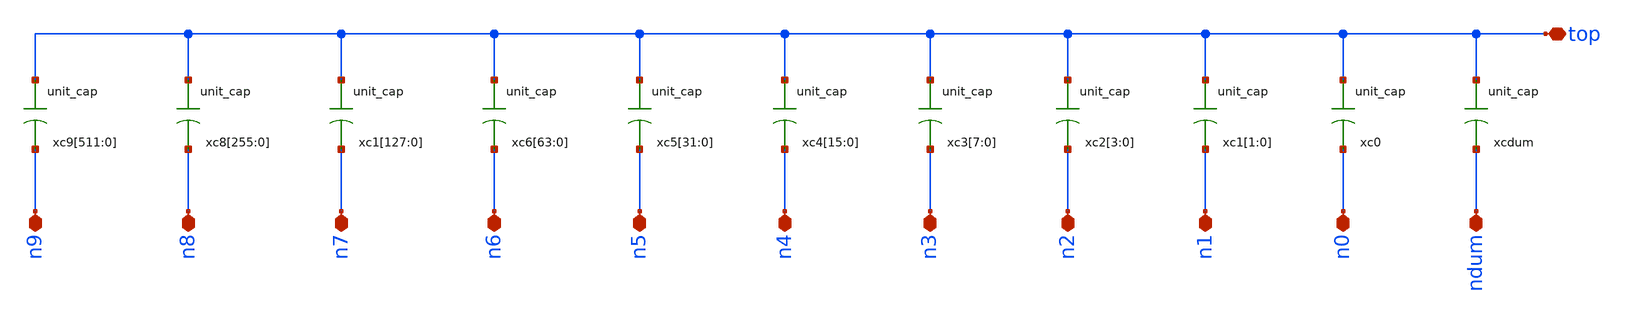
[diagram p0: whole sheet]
** sch_path: xschem/adc/carry.sch
**.subckt carry n9 n8 n7 n6 n5 n4 n3 n2 n1 n0 ndum top
*.iopin n9
*.iopin n8
*.iopin n7
*.iopin n6
*.iopin n5
*.iopin n4
*.iopin n3
*.iopin n2
*.iopin n1
*.iopin n0
*.iopin ndum
*.iopin top
xc9[511] top n9 unit_cap
xc9[510] top n9 unit_cap
xc9[509] top n9 unit_cap
xc9[508] top n9 unit_cap
xc9[507] top n9 unit_cap
xc9[506] top n9 unit_cap
xc9[505] top n9 unit_cap
xc9[504] top n9 unit_cap
xc9[503] top n9 unit_cap
xc9[502] top n9 unit_cap
xc9[501] top n9 unit_cap
xc9[500] top n9 unit_cap
xc9[499] top n9 unit_cap
xc9[498] top n9 unit_cap
xc9[497] top n9 unit_cap
xc9[496] top n9 unit_cap
xc9[495] top n9 unit_cap
xc9[494] top n9 unit_cap
xc9[493] top n9 unit_cap
xc9[492] top n9 unit_cap
xc9[491] top n9 unit_cap
xc9[490] top n9 unit_cap
xc9[489] top n9 unit_cap
xc9[488] top n9 unit_cap
xc9[487] top n9 unit_cap
xc9[486] top n9 unit_cap
xc9[485] top n9 unit_cap
xc9[484] top n9 unit_cap
xc9[483] top n9 unit_cap
xc9[482] top n9 unit_cap
xc9[481] top n9 unit_cap
xc9[480] top n9 unit_cap
xc9[479] top n9 unit_cap
xc9[478] top n9 unit_cap
xc9[477] top n9 unit_cap
xc9[476] top n9 unit_cap
xc9[475] top n9 unit_cap
xc9[474] top n9 unit_cap
xc9[473] top n9 unit_cap
xc9[472] top n9 unit_cap
xc9[471] top n9 unit_cap
xc9[470] top n9 unit_cap
xc9[469] top n9 unit_cap
xc9[468] top n9 unit_cap
xc9[467] top n9 unit_cap
xc9[466] top n9 unit_cap
xc9[465] top n9 unit_cap
xc9[464] top n9 unit_cap
xc9[463] top n9 unit_cap
xc9[462] top n9 unit_cap
xc9[461] top n9 unit_cap
xc9[460] top n9 unit_cap
xc9[459] top n9 unit_cap
xc9[458] top n9 unit_cap
xc9[457] top n9 unit_cap
xc9[456] top n9 unit_cap
xc9[455] top n9 unit_cap
xc9[454] top n9 unit_cap
xc9[453] top n9 unit_cap
xc9[452] top n9 unit_cap
xc9[451] top n9 unit_cap
xc9[450] top n9 unit_cap
xc9[449] top n9 unit_cap
xc9[448] top n9 unit_cap
xc9[447] top n9 unit_cap
xc9[446] top n9 unit_cap
xc9[445] top n9 unit_cap
xc9[444] top n9 unit_cap
xc9[443] top n9 unit_cap
xc9[442] top n9 unit_cap
xc9[441] top n9 unit_cap
xc9[440] top n9 unit_cap
xc9[439] top n9 unit_cap
xc9[438] top n9 unit_cap
xc9[437] top n9 unit_cap
xc9[436] top n9 unit_cap
xc9[435] top n9 unit_cap
xc9[434] top n9 unit_cap
xc9[433] top n9 unit_cap
xc9[432] top n9 unit_cap
xc9[431] top n9 unit_cap
xc9[430] top n9 unit_cap
xc9[429] top n9 unit_cap
xc9[428] top n9 unit_cap
xc9[427] top n9 unit_cap
xc9[426] top n9 unit_cap
xc9[425] top n9 unit_cap
xc9[424] top n9 unit_cap
xc9[423] top n9 unit_cap
xc9[422] top n9 unit_cap
xc9[421] top n9 unit_cap
xc9[420] top n9 unit_cap
xc9[419] top n9 unit_cap
xc9[418] top n9 unit_cap
xc9[417] top n9 unit_cap
xc9[416] top n9 unit_cap
xc9[415] top n9 unit_cap
xc9[414] top n9 unit_cap
xc9[413] top n9 unit_cap
xc9[412] top n9 unit_cap
xc9[411] top n9 unit_cap
xc9[410] top n9 unit_cap
xc9[409] top n9 unit_cap
xc9[408] top n9 unit_cap
xc9[407] top n9 unit_cap
xc9[406] top n9 unit_cap
xc9[405] top n9 unit_cap
xc9[404] top n9 unit_cap
xc9[403] top n9 unit_cap
xc9[402] top n9 unit_cap
xc9[401] top n9 unit_cap
xc9[400] top n9 unit_cap
xc9[399] top n9 unit_cap
xc9[398] top n9 unit_cap
xc9[397] top n9 unit_cap
xc9[396] top n9 unit_cap
xc9[395] top n9 unit_cap
xc9[394] top n9 unit_cap
xc9[393] top n9 unit_cap
xc9[392] top n9 unit_cap
xc9[391] top n9 unit_cap
xc9[390] top n9 unit_cap
xc9[389] top n9 unit_cap
xc9[388] top n9 unit_cap
xc9[387] top n9 unit_cap
xc9[386] top n9 unit_cap
xc9[385] top n9 unit_cap
xc9[384] top n9 unit_cap
xc9[383] top n9 unit_cap
xc9[382] top n9 unit_cap
xc9[381] top n9 unit_cap
xc9[380] top n9 unit_cap
xc9[379] top n9 unit_cap
xc9[378] top n9 unit_cap
xc9[377] top n9 unit_cap
xc9[376] top n9 unit_cap
xc9[375] top n9 unit_cap
xc9[374] top n9 unit_cap
xc9[373] top n9 unit_cap
xc9[372] top n9 unit_cap
xc9[371] top n9 unit_cap
xc9[370] top n9 unit_cap
xc9[369] top n9 unit_cap
xc9[368] top n9 unit_cap
xc9[367] top n9 unit_cap
xc9[366] top n9 unit_cap
xc9[365] top n9 unit_cap
xc9[364] top n9 unit_cap
xc9[363] top n9 unit_cap
xc9[362] top n9 unit_cap
xc9[361] top n9 unit_cap
xc9[360] top n9 unit_cap
xc9[359] top n9 unit_cap
xc9[358] top n9 unit_cap
xc9[357] top n9 unit_cap
xc9[356] top n9 unit_cap
xc9[355] top n9 unit_cap
xc9[354] top n9 unit_cap
xc9[353] top n9 unit_cap
xc9[352] top n9 unit_cap
xc9[351] top n9 unit_cap
xc9[350] top n9 unit_cap
xc9[349] top n9 unit_cap
xc9[348] top n9 unit_cap
xc9[347] top n9 unit_cap
xc9[346] top n9 unit_cap
xc9[345] top n9 unit_cap
xc9[344] top n9 unit_cap
xc9[343] top n9 unit_cap
xc9[342] top n9 unit_cap
xc9[341] top n9 unit_cap
xc9[340] top n9 unit_cap
xc9[339] top n9 unit_cap
xc9[338] top n9 unit_cap
xc9[337] top n9 unit_cap
xc9[336] top n9 unit_cap
xc9[335] top n9 unit_cap
xc9[334] top n9 unit_cap
xc9[333] top n9 unit_cap
xc9[332] top n9 unit_cap
xc9[331] top n9 unit_cap
xc9[330] top n9 unit_cap
xc9[329] top n9 unit_cap
xc9[328] top n9 unit_cap
xc9[327] top n9 unit_cap
xc9[326] top n9 unit_cap
xc9[325] top n9 unit_cap
xc9[324] top n9 unit_cap
xc9[323] top n9 unit_cap
xc9[322] top n9 unit_cap
xc9[321] top n9 unit_cap
xc9[320] top n9 unit_cap
xc9[319] top n9 unit_cap
xc9[318] top n9 unit_cap
xc9[317] top n9 unit_cap
xc9[316] top n9 unit_cap
xc9[315] top n9 unit_cap
xc9[314] top n9 unit_cap
xc9[313] top n9 unit_cap
xc9[312] top n9 unit_cap
xc9[311] top n9 unit_cap
xc9[310] top n9 unit_cap
xc9[309] top n9 unit_cap
xc9[308] top n9 unit_cap
xc9[307] top n9 unit_cap
xc9[306] top n9 unit_cap
xc9[305] top n9 unit_cap
xc9[304] top n9 unit_cap
xc9[303] top n9 unit_cap
xc9[302] top n9 unit_cap
xc9[301] top n9 unit_cap
xc9[300] top n9 unit_cap
xc9[299] top n9 unit_cap
xc9[298] top n9 unit_cap
xc9[297] top n9 unit_cap
xc9[296] top n9 unit_cap
xc9[295] top n9 unit_cap
xc9[294] top n9 unit_cap
xc9[293] top n9 unit_cap
xc9[292] top n9 unit_cap
xc9[291] top n9 unit_cap
xc9[290] top n9 unit_cap
xc9[289] top n9 unit_cap
xc9[288] top n9 unit_cap
xc9[287] top n9 unit_cap
xc9[286] top n9 unit_cap
xc9[285] top n9 unit_cap
xc9[284] top n9 unit_cap
xc9[283] top n9 unit_cap
xc9[282] top n9 unit_cap
xc9[281] top n9 unit_cap
xc9[280] top n9 unit_cap
xc9[279] top n9 unit_cap
xc9[278] top n9 unit_cap
xc9[277] top n9 unit_cap
xc9[276] top n9 unit_cap
xc9[275] top n9 unit_cap
xc9[274] top n9 unit_cap
xc9[273] top n9 unit_cap
xc9[272] top n9 unit_cap
xc9[271] top n9 unit_cap
xc9[270] top n9 unit_cap
xc9[269] top n9 unit_cap
xc9[268] top n9 unit_cap
xc9[267] top n9 unit_cap
xc9[266] top n9 unit_cap
xc9[265] top n9 unit_cap
xc9[264] top n9 unit_cap
xc9[263] top n9 unit_cap
xc9[262] top n9 unit_cap
xc9[261] top n9 unit_cap
xc9[260] top n9 unit_cap
xc9[259] top n9 unit_cap
xc9[258] top n9 unit_cap
xc9[257] top n9 unit_cap
xc9[256] top n9 unit_cap
xc9[255] top n9 unit_cap
xc9[254] top n9 unit_cap
xc9[253] top n9 unit_cap
xc9[252] top n9 unit_cap
xc9[251] top n9 unit_cap
xc9[250] top n9 unit_cap
xc9[249] top n9 unit_cap
xc9[248] top n9 unit_cap
xc9[247] top n9 unit_cap
xc9[246] top n9 unit_cap
xc9[245] top n9 unit_cap
xc9[244] top n9 unit_cap
xc9[243] top n9 unit_cap
xc9[242] top n9 unit_cap
xc9[241] top n9 unit_cap
xc9[240] top n9 unit_cap
xc9[239] top n9 unit_cap
xc9[238] top n9 unit_cap
xc9[237] top n9 unit_cap
xc9[236] top n9 unit_cap
xc9[235] top n9 unit_cap
xc9[234] top n9 unit_cap
xc9[233] top n9 unit_cap
xc9[232] top n9 unit_cap
xc9[231] top n9 unit_cap
xc9[230] top n9 unit_cap
xc9[229] top n9 unit_cap
xc9[228] top n9 unit_cap
xc9[227] top n9 unit_cap
xc9[226] top n9 unit_cap
xc9[225] top n9 unit_cap
xc9[224] top n9 unit_cap
xc9[223] top n9 unit_cap
xc9[222] top n9 unit_cap
xc9[221] top n9 unit_cap
xc9[220] top n9 unit_cap
xc9[219] top n9 unit_cap
xc9[218] top n9 unit_cap
xc9[217] top n9 unit_cap
xc9[216] top n9 unit_cap
xc9[215] top n9 unit_cap
xc9[214] top n9 unit_cap
xc9[213] top n9 unit_cap
xc9[212] top n9 unit_cap
xc9[211] top n9 unit_cap
xc9[210] top n9 unit_cap
xc9[209] top n9 unit_cap
xc9[208] top n9 unit_cap
xc9[207] top n9 unit_cap
xc9[206] top n9 unit_cap
xc9[205] top n9 unit_cap
xc9[204] top n9 unit_cap
xc9[203] top n9 unit_cap
xc9[202] top n9 unit_cap
xc9[201] top n9 unit_cap
xc9[200] top n9 unit_cap
xc9[199] top n9 unit_cap
xc9[198] top n9 unit_cap
xc9[197] top n9 unit_cap
xc9[196] top n9 unit_cap
xc9[195] top n9 unit_cap
xc9[194] top n9 unit_cap
xc9[193] top n9 unit_cap
xc9[192] top n9 unit_cap
xc9[191] top n9 unit_cap
xc9[190] top n9 unit_cap
xc9[189] top n9 unit_cap
xc9[188] top n9 unit_cap
xc9[187] top n9 unit_cap
xc9[186] top n9 unit_cap
xc9[185] top n9 unit_cap
xc9[184] top n9 unit_cap
xc9[183] top n9 unit_cap
xc9[182] top n9 unit_cap
xc9[181] top n9 unit_cap
xc9[180] top n9 unit_cap
xc9[179] top n9 unit_cap
xc9[178] top n9 unit_cap
xc9[177] top n9 unit_cap
xc9[176] top n9 unit_cap
xc9[175] top n9 unit_cap
xc9[174] top n9 unit_cap
xc9[173] top n9 unit_cap
xc9[172] top n9 unit_cap
xc9[171] top n9 unit_cap
xc9[170] top n9 unit_cap
xc9[169] top n9 unit_cap
xc9[168] top n9 unit_cap
xc9[167] top n9 unit_cap
xc9[166] top n9 unit_cap
xc9[165] top n9 unit_cap
xc9[164] top n9 unit_cap
xc9[163] top n9 unit_cap
xc9[162] top n9 unit_cap
xc9[161] top n9 unit_cap
xc9[160] top n9 unit_cap
xc9[159] top n9 unit_cap
xc9[158] top n9 unit_cap
xc9[157] top n9 unit_cap
xc9[156] top n9 unit_cap
xc9[155] top n9 unit_cap
xc9[154] top n9 unit_cap
xc9[153] top n9 unit_cap
xc9[152] top n9 unit_cap
xc9[151] top n9 unit_cap
xc9[150] top n9 unit_cap
xc9[149] top n9 unit_cap
xc9[148] top n9 unit_cap
xc9[147] top n9 unit_cap
xc9[146] top n9 unit_cap
xc9[145] top n9 unit_cap
xc9[144] top n9 unit_cap
xc9[143] top n9 unit_cap
xc9[142] top n9 unit_cap
xc9[141] top n9 unit_cap
xc9[140] top n9 unit_cap
xc9[139] top n9 unit_cap
xc9[138] top n9 unit_cap
xc9[137] top n9 unit_cap
xc9[136] top n9 unit_cap
xc9[135] top n9 unit_cap
xc9[134] top n9 unit_cap
xc9[133] top n9 unit_cap
xc9[132] top n9 unit_cap
xc9[131] top n9 unit_cap
xc9[130] top n9 unit_cap
xc9[129] top n9 unit_cap
xc9[128] top n9 unit_cap
xc9[127] top n9 unit_cap
xc9[126] top n9 unit_cap
xc9[125] top n9 unit_cap
xc9[124] top n9 unit_cap
xc9[123] top n9 unit_cap
xc9[122] top n9 unit_cap
xc9[121] top n9 unit_cap
xc9[120] top n9 unit_cap
xc9[119] top n9 unit_cap
xc9[118] top n9 unit_cap
xc9[117] top n9 unit_cap
xc9[116] top n9 unit_cap
xc9[115] top n9 unit_cap
xc9[114] top n9 unit_cap
xc9[113] top n9 unit_cap
xc9[112] top n9 unit_cap
xc9[111] top n9 unit_cap
xc9[110] top n9 unit_cap
xc9[109] top n9 unit_cap
xc9[108] top n9 unit_cap
xc9[107] top n9 unit_cap
xc9[106] top n9 unit_cap
xc9[105] top n9 unit_cap
xc9[104] top n9 unit_cap
xc9[103] top n9 unit_cap
xc9[102] top n9 unit_cap
xc9[101] top n9 unit_cap
xc9[100] top n9 unit_cap
xc9[99] top n9 unit_cap
xc9[98] top n9 unit_cap
xc9[97] top n9 unit_cap
xc9[96] top n9 unit_cap
xc9[95] top n9 unit_cap
xc9[94] top n9 unit_cap
xc9[93] top n9 unit_cap
xc9[92] top n9 unit_cap
xc9[91] top n9 unit_cap
xc9[90] top n9 unit_cap
xc9[89] top n9 unit_cap
xc9[88] top n9 unit_cap
xc9[87] top n9 unit_cap
xc9[86] top n9 unit_cap
xc9[85] top n9 unit_cap
xc9[84] top n9 unit_cap
xc9[83] top n9 unit_cap
xc9[82] top n9 unit_cap
xc9[81] top n9 unit_cap
xc9[80] top n9 unit_cap
xc9[79] top n9 unit_cap
xc9[78] top n9 unit_cap
xc9[77] top n9 unit_cap
xc9[76] top n9 unit_cap
xc9[75] top n9 unit_cap
xc9[74] top n9 unit_cap
xc9[73] top n9 unit_cap
xc9[72] top n9 unit_cap
xc9[71] top n9 unit_cap
xc9[70] top n9 unit_cap
xc9[69] top n9 unit_cap
xc9[68] top n9 unit_cap
xc9[67] top n9 unit_cap
xc9[66] top n9 unit_cap
xc9[65] top n9 unit_cap
xc9[64] top n9 unit_cap
xc9[63] top n9 unit_cap
xc9[62] top n9 unit_cap
xc9[61] top n9 unit_cap
xc9[60] top n9 unit_cap
xc9[59] top n9 unit_cap
xc9[58] top n9 unit_cap
xc9[57] top n9 unit_cap
xc9[56] top n9 unit_cap
xc9[55] top n9 unit_cap
xc9[54] top n9 unit_cap
xc9[53] top n9 unit_cap
xc9[52] top n9 unit_cap
xc9[51] top n9 unit_cap
xc9[50] top n9 unit_cap
xc9[49] top n9 unit_cap
xc9[48] top n9 unit_cap
xc9[47] top n9 unit_cap
xc9[46] top n9 unit_cap
xc9[45] top n9 unit_cap
xc9[44] top n9 unit_cap
xc9[43] top n9 unit_cap
xc9[42] top n9 unit_cap
xc9[41] top n9 unit_cap
xc9[40] top n9 unit_cap
xc9[39] top n9 unit_cap
xc9[38] top n9 unit_cap
xc9[37] top n9 unit_cap
xc9[36] top n9 unit_cap
xc9[35] top n9 unit_cap
xc9[34] top n9 unit_cap
xc9[33] top n9 unit_cap
xc9[32] top n9 unit_cap
xc9[31] top n9 unit_cap
xc9[30] top n9 unit_cap
xc9[29] top n9 unit_cap
xc9[28] top n9 unit_cap
xc9[27] top n9 unit_cap
xc9[26] top n9 unit_cap
xc9[25] top n9 unit_cap
xc9[24] top n9 unit_cap
xc9[23] top n9 unit_cap
xc9[22] top n9 unit_cap
xc9[21] top n9 unit_cap
xc9[20] top n9 unit_cap
xc9[19] top n9 unit_cap
xc9[18] top n9 unit_cap
xc9[17] top n9 unit_cap
xc9[16] top n9 unit_cap
xc9[15] top n9 unit_cap
xc9[14] top n9 unit_cap
xc9[13] top n9 unit_cap
xc9[12] top n9 unit_cap
xc9[11] top n9 unit_cap
xc9[10] top n9 unit_cap
xc9[9] top n9 unit_cap
xc9[8] top n9 unit_cap
xc9[7] top n9 unit_cap
xc9[6] top n9 unit_cap
xc9[5] top n9 unit_cap
xc9[4] top n9 unit_cap
xc9[3] top n9 unit_cap
xc9[2] top n9 unit_cap
xc9[1] top n9 unit_cap
xc9[0] top n9 unit_cap
xc8[255] top n8 unit_cap
xc8[254] top n8 unit_cap
xc8[253] top n8 unit_cap
xc8[252] top n8 unit_cap
xc8[251] top n8 unit_cap
xc8[250] top n8 unit_cap
xc8[249] top n8 unit_cap
xc8[248] top n8 unit_cap
xc8[247] top n8 unit_cap
xc8[246] top n8 unit_cap
xc8[245] top n8 unit_cap
xc8[244] top n8 unit_cap
xc8[243] top n8 unit_cap
xc8[242] top n8 unit_cap
xc8[241] top n8 unit_cap
xc8[240] top n8 unit_cap
xc8[239] top n8 unit_cap
xc8[238] top n8 unit_cap
xc8[237] top n8 unit_cap
xc8[236] top n8 unit_cap
xc8[235] top n8 unit_cap
xc8[234] top n8 unit_cap
xc8[233] top n8 unit_cap
xc8[232] top n8 unit_cap
xc8[231] top n8 unit_cap
xc8[230] top n8 unit_cap
xc8[229] top n8 unit_cap
xc8[228] top n8 unit_cap
xc8[227] top n8 unit_cap
xc8[226] top n8 unit_cap
xc8[225] top n8 unit_cap
xc8[224] top n8 unit_cap
xc8[223] top n8 unit_cap
xc8[222] top n8 unit_cap
xc8[221] top n8 unit_cap
xc8[220] top n8 unit_cap
xc8[219] top n8 unit_cap
xc8[218] top n8 unit_cap
xc8[217] top n8 unit_cap
xc8[216] top n8 unit_cap
xc8[215] top n8 unit_cap
xc8[214] top n8 unit_cap
xc8[213] top n8 unit_cap
xc8[212] top n8 unit_cap
xc8[211] top n8 unit_cap
xc8[210] top n8 unit_cap
xc8[209] top n8 unit_cap
xc8[208] top n8 unit_cap
xc8[207] top n8 unit_cap
xc8[206] top n8 unit_cap
xc8[205] top n8 unit_cap
xc8[204] top n8 unit_cap
xc8[203] top n8 unit_cap
xc8[202] top n8 unit_cap
xc8[201] top n8 unit_cap
xc8[200] top n8 unit_cap
xc8[199] top n8 unit_cap
xc8[198] top n8 unit_cap
xc8[197] top n8 unit_cap
xc8[196] top n8 unit_cap
xc8[195] top n8 unit_cap
xc8[194] top n8 unit_cap
xc8[193] top n8 unit_cap
xc8[192] top n8 unit_cap
xc8[191] top n8 unit_cap
xc8[190] top n8 unit_cap
xc8[189] top n8 unit_cap
xc8[188] top n8 unit_cap
xc8[187] top n8 unit_cap
xc8[186] top n8 unit_cap
xc8[185] top n8 unit_cap
xc8[184] top n8 unit_cap
xc8[183] top n8 unit_cap
xc8[182] top n8 unit_cap
xc8[181] top n8 unit_cap
xc8[180] top n8 unit_cap
xc8[179] top n8 unit_cap
xc8[178] top n8 unit_cap
xc8[177] top n8 unit_cap
xc8[176] top n8 unit_cap
xc8[175] top n8 unit_cap
xc8[174] top n8 unit_cap
xc8[173] top n8 unit_cap
xc8[172] top n8 unit_cap
xc8[171] top n8 unit_cap
xc8[170] top n8 unit_cap
xc8[169] top n8 unit_cap
xc8[168] top n8 unit_cap
xc8[167] top n8 unit_cap
xc8[166] top n8 unit_cap
xc8[165] top n8 unit_cap
xc8[164] top n8 unit_cap
xc8[163] top n8 unit_cap
xc8[162] top n8 unit_cap
xc8[161] top n8 unit_cap
xc8[160] top n8 unit_cap
xc8[159] top n8 unit_cap
xc8[158] top n8 unit_cap
xc8[157] top n8 unit_cap
xc8[156] top n8 unit_cap
xc8[155] top n8 unit_cap
xc8[154] top n8 unit_cap
xc8[153] top n8 unit_cap
xc8[152] top n8 unit_cap
xc8[151] top n8 unit_cap
xc8[150] top n8 unit_cap
xc8[149] top n8 unit_cap
xc8[148] top n8 unit_cap
xc8[147] top n8 unit_cap
xc8[146] top n8 unit_cap
xc8[145] top n8 unit_cap
xc8[144] top n8 unit_cap
xc8[143] top n8 unit_cap
xc8[142] top n8 unit_cap
xc8[141] top n8 unit_cap
xc8[140] top n8 unit_cap
xc8[139] top n8 unit_cap
xc8[138] top n8 unit_cap
xc8[137] top n8 unit_cap
xc8[136] top n8 unit_cap
xc8[135] top n8 unit_cap
xc8[134] top n8 unit_cap
xc8[133] top n8 unit_cap
xc8[132] top n8 unit_cap
xc8[131] top n8 unit_cap
xc8[130] top n8 unit_cap
xc8[129] top n8 unit_cap
xc8[128] top n8 unit_cap
xc8[127] top n8 unit_cap
xc8[126] top n8 unit_cap
xc8[125] top n8 unit_cap
xc8[124] top n8 unit_cap
xc8[123] top n8 unit_cap
xc8[122] top n8 unit_cap
xc8[121] top n8 unit_cap
xc8[120] top n8 unit_cap
xc8[119] top n8 unit_cap
xc8[118] top n8 unit_cap
xc8[117] top n8 unit_cap
xc8[116] top n8 unit_cap
xc8[115] top n8 unit_cap
xc8[114] top n8 unit_cap
xc8[113] top n8 unit_cap
xc8[112] top n8 unit_cap
xc8[111] top n8 unit_cap
xc8[110] top n8 unit_cap
xc8[109] top n8 unit_cap
xc8[108] top n8 unit_cap
xc8[107] top n8 unit_cap
xc8[106] top n8 unit_cap
xc8[105] top n8 unit_cap
xc8[104] top n8 unit_cap
xc8[103] top n8 unit_cap
xc8[102] top n8 unit_cap
xc8[101] top n8 unit_cap
xc8[100] top n8 unit_cap
xc8[99] top n8 unit_cap
xc8[98] top n8 unit_cap
xc8[97] top n8 unit_cap
xc8[96] top n8 unit_cap
xc8[95] top n8 unit_cap
xc8[94] top n8 unit_cap
xc8[93] top n8 unit_cap
xc8[92] top n8 unit_cap
xc8[91] top n8 unit_cap
xc8[90] top n8 unit_cap
xc8[89] top n8 unit_cap
xc8[88] top n8 unit_cap
xc8[87] top n8 unit_cap
xc8[86] top n8 unit_cap
xc8[85] top n8 unit_cap
xc8[84] top n8 unit_cap
xc8[83] top n8 unit_cap
xc8[82] top n8 unit_cap
xc8[81] top n8 unit_cap
xc8[80] top n8 unit_cap
xc8[79] top n8 unit_cap
xc8[78] top n8 unit_cap
xc8[77] top n8 unit_cap
xc8[76] top n8 unit_cap
xc8[75] top n8 unit_cap
xc8[74] top n8 unit_cap
xc8[73] top n8 unit_cap
xc8[72] top n8 unit_cap
xc8[71] top n8 unit_cap
xc8[70] top n8 unit_cap
xc8[69] top n8 unit_cap
xc8[68] top n8 unit_cap
xc8[67] top n8 unit_cap
xc8[66] top n8 unit_cap
xc8[65] top n8 unit_cap
xc8[64] top n8 unit_cap
xc8[63] top n8 unit_cap
xc8[62] top n8 unit_cap
xc8[61] top n8 unit_cap
xc8[60] top n8 unit_cap
xc8[59] top n8 unit_cap
xc8[58] top n8 unit_cap
xc8[57] top n8 unit_cap
xc8[56] top n8 unit_cap
xc8[55] top n8 unit_cap
xc8[54] top n8 unit_cap
xc8[53] top n8 unit_cap
xc8[52] top n8 unit_cap
xc8[51] top n8 unit_cap
xc8[50] top n8 unit_cap
xc8[49] top n8 unit_cap
xc8[48] top n8 unit_cap
xc8[47] top n8 unit_cap
xc8[46] top n8 unit_cap
xc8[45] top n8 unit_cap
xc8[44] top n8 unit_cap
xc8[43] top n8 unit_cap
xc8[42] top n8 unit_cap
xc8[41] top n8 unit_cap
xc8[40] top n8 unit_cap
xc8[39] top n8 unit_cap
xc8[38] top n8 unit_cap
xc8[37] top n8 unit_cap
xc8[36] top n8 unit_cap
xc8[35] top n8 unit_cap
xc8[34] top n8 unit_cap
xc8[33] top n8 unit_cap
xc8[32] top n8 unit_cap
xc8[31] top n8 unit_cap
xc8[30] top n8 unit_cap
xc8[29] top n8 unit_cap
xc8[28] top n8 unit_cap
xc8[27] top n8 unit_cap
xc8[26] top n8 unit_cap
xc8[25] top n8 unit_cap
xc8[24] top n8 unit_cap
xc8[23] top n8 unit_cap
xc8[22] top n8 unit_cap
xc8[21] top n8 unit_cap
xc8[20] top n8 unit_cap
xc8[19] top n8 unit_cap
xc8[18] top n8 unit_cap
xc8[17] top n8 unit_cap
xc8[16] top n8 unit_cap
xc8[15] top n8 unit_cap
xc8[14] top n8 unit_cap
xc8[13] top n8 unit_cap
xc8[12] top n8 unit_cap
xc8[11] top n8 unit_cap
xc8[10] top n8 unit_cap
xc8[9] top n8 unit_cap
xc8[8] top n8 unit_cap
xc8[7] top n8 unit_cap
xc8[6] top n8 unit_cap
xc8[5] top n8 unit_cap
xc8[4] top n8 unit_cap
xc8[3] top n8 unit_cap
xc8[2] top n8 unit_cap
xc8[1] top n8 unit_cap
xc8[0] top n8 unit_cap
xc0 top n0 unit_cap
xcdum top ndum unit_cap
xc1[1] top n1 unit_cap
xc1[0] top n1 unit_cap
xc2[3] top n2 unit_cap
xc2[2] top n2 unit_cap
xc2[1] top n2 unit_cap
xc2[0] top n2 unit_cap
xc3[7] top n3 unit_cap
xc3[6] top n3 unit_cap
xc3[5] top n3 unit_cap
xc3[4] top n3 unit_cap
xc3[3] top n3 unit_cap
xc3[2] top n3 unit_cap
xc3[1] top n3 unit_cap
xc3[0] top n3 unit_cap
xc4[15] top n4 unit_cap
xc4[14] top n4 unit_cap
xc4[13] top n4 unit_cap
xc4[12] top n4 unit_cap
xc4[11] top n4 unit_cap
xc4[10] top n4 unit_cap
xc4[9] top n4 unit_cap
xc4[8] top n4 unit_cap
xc4[7] top n4 unit_cap
xc4[6] top n4 unit_cap
xc4[5] top n4 unit_cap
xc4[4] top n4 unit_cap
xc4[3] top n4 unit_cap
xc4[2] top n4 unit_cap
xc4[1] top n4 unit_cap
xc4[0] top n4 unit_cap
xc5[31] top n5 unit_cap
xc5[30] top n5 unit_cap
xc5[29] top n5 unit_cap
xc5[28] top n5 unit_cap
xc5[27] top n5 unit_cap
xc5[26] top n5 unit_cap
xc5[25] top n5 unit_cap
xc5[24] top n5 unit_cap
xc5[23] top n5 unit_cap
xc5[22] top n5 unit_cap
xc5[21] top n5 unit_cap
xc5[20] top n5 unit_cap
xc5[19] top n5 unit_cap
xc5[18] top n5 unit_cap
xc5[17] top n5 unit_cap
xc5[16] top n5 unit_cap
xc5[15] top n5 unit_cap
xc5[14] top n5 unit_cap
xc5[13] top n5 unit_cap
xc5[12] top n5 unit_cap
xc5[11] top n5 unit_cap
xc5[10] top n5 unit_cap
xc5[9] top n5 unit_cap
xc5[8] top n5 unit_cap
xc5[7] top n5 unit_cap
xc5[6] top n5 unit_cap
xc5[5] top n5 unit_cap
xc5[4] top n5 unit_cap
xc5[3] top n5 unit_cap
xc5[2] top n5 unit_cap
xc5[1] top n5 unit_cap
xc5[0] top n5 unit_cap
xc6[63] top n6 unit_cap
xc6[62] top n6 unit_cap
xc6[61] top n6 unit_cap
xc6[60] top n6 unit_cap
xc6[59] top n6 unit_cap
xc6[58] top n6 unit_cap
xc6[57] top n6 unit_cap
xc6[56] top n6 unit_cap
xc6[55] top n6 unit_cap
xc6[54] top n6 unit_cap
xc6[53] top n6 unit_cap
xc6[52] top n6 unit_cap
xc6[51] top n6 unit_cap
xc6[50] top n6 unit_cap
xc6[49] top n6 unit_cap
xc6[48] top n6 unit_cap
xc6[47] top n6 unit_cap
xc6[46] top n6 unit_cap
xc6[45] top n6 unit_cap
xc6[44] top n6 unit_cap
xc6[43] top n6 unit_cap
xc6[42] top n6 unit_cap
xc6[41] top n6 unit_cap
xc6[40] top n6 unit_cap
xc6[39] top n6 unit_cap
xc6[38] top n6 unit_cap
xc6[37] top n6 unit_cap
xc6[36] top n6 unit_cap
xc6[35] top n6 unit_cap
xc6[34] top n6 unit_cap
xc6[33] top n6 unit_cap
xc6[32] top n6 unit_cap
xc6[31] top n6 unit_cap
xc6[30] top n6 unit_cap
xc6[29] top n6 unit_cap
xc6[28] top n6 unit_cap
xc6[27] top n6 unit_cap
xc6[26] top n6 unit_cap
xc6[25] top n6 unit_cap
xc6[24] top n6 unit_cap
xc6[23] top n6 unit_cap
xc6[22] top n6 unit_cap
xc6[21] top n6 unit_cap
xc6[20] top n6 unit_cap
xc6[19] top n6 unit_cap
xc6[18] top n6 unit_cap
xc6[17] top n6 unit_cap
xc6[16] top n6 unit_cap
xc6[15] top n6 unit_cap
xc6[14] top n6 unit_cap
xc6[13] top n6 unit_cap
xc6[12] top n6 unit_cap
xc6[11] top n6 unit_cap
xc6[10] top n6 unit_cap
xc6[9] top n6 unit_cap
xc6[8] top n6 unit_cap
xc6[7] top n6 unit_cap
xc6[6] top n6 unit_cap
xc6[5] top n6 unit_cap
xc6[4] top n6 unit_cap
xc6[3] top n6 unit_cap
xc6[2] top n6 unit_cap
xc6[1] top n6 unit_cap
xc6[0] top n6 unit_cap
xc1[127] top n7 unit_cap
xc1[126] top n7 unit_cap
xc1[125] top n7 unit_cap
xc1[124] top n7 unit_cap
xc1[123] top n7 unit_cap
xc1[122] top n7 unit_cap
xc1[121] top n7 unit_cap
xc1[120] top n7 unit_cap
xc1[119] top n7 unit_cap
xc1[118] top n7 unit_cap
xc1[117] top n7 unit_cap
xc1[116] top n7 unit_cap
xc1[115] top n7 unit_cap
xc1[114] top n7 unit_cap
xc1[113] top n7 unit_cap
xc1[112] top n7 unit_cap
xc1[111] top n7 unit_cap
xc1[110] top n7 unit_cap
xc1[109] top n7 unit_cap
xc1[108] top n7 unit_cap
xc1[107] top n7 unit_cap
xc1[106] top n7 unit_cap
xc1[105] top n7 unit_cap
xc1[104] top n7 unit_cap
xc1[103] top n7 unit_cap
xc1[102] top n7 unit_cap
xc1[101] top n7 unit_cap
xc1[100] top n7 unit_cap
xc1[99] top n7 unit_cap
xc1[98] top n7 unit_cap
xc1[97] top n7 unit_cap
xc1[96] top n7 unit_cap
xc1[95] top n7 unit_cap
xc1[94] top n7 unit_cap
xc1[93] top n7 unit_cap
xc1[92] top n7 unit_cap
xc1[91] top n7 unit_cap
xc1[90] top n7 unit_cap
xc1[89] top n7 unit_cap
xc1[88] top n7 unit_cap
xc1[87] top n7 unit_cap
xc1[86] top n7 unit_cap
xc1[85] top n7 unit_cap
xc1[84] top n7 unit_cap
xc1[83] top n7 unit_cap
xc1[82] top n7 unit_cap
xc1[81] top n7 unit_cap
xc1[80] top n7 unit_cap
xc1[79] top n7 unit_cap
xc1[78] top n7 unit_cap
xc1[77] top n7 unit_cap
xc1[76] top n7 unit_cap
xc1[75] top n7 unit_cap
xc1[74] top n7 unit_cap
xc1[73] top n7 unit_cap
xc1[72] top n7 unit_cap
xc1[71] top n7 unit_cap
xc1[70] top n7 unit_cap
xc1[69] top n7 unit_cap
xc1[68] top n7 unit_cap
xc1[67] top n7 unit_cap
xc1[66] top n7 unit_cap
xc1[65] top n7 unit_cap
xc1[64] top n7 unit_cap
xc1[63] top n7 unit_cap
xc1[62] top n7 unit_cap
xc1[61] top n7 unit_cap
xc1[60] top n7 unit_cap
xc1[59] top n7 unit_cap
xc1[58] top n7 unit_cap
xc1[57] top n7 unit_cap
xc1[56] top n7 unit_cap
xc1[55] top n7 unit_cap
xc1[54] top n7 unit_cap
xc1[53] top n7 unit_cap
xc1[52] top n7 unit_cap
xc1[51] top n7 unit_cap
xc1[50] top n7 unit_cap
xc1[49] top n7 unit_cap
xc1[48] top n7 unit_cap
xc1[47] top n7 unit_cap
xc1[46] top n7 unit_cap
xc1[45] top n7 unit_cap
xc1[44] top n7 unit_cap
xc1[43] top n7 unit_cap
xc1[42] top n7 unit_cap
xc1[41] top n7 unit_cap
xc1[40] top n7 unit_cap
xc1[39] top n7 unit_cap
xc1[38] top n7 unit_cap
xc1[37] top n7 unit_cap
xc1[36] top n7 unit_cap
xc1[35] top n7 unit_cap
xc1[34] top n7 unit_cap
xc1[33] top n7 unit_cap
xc1[32] top n7 unit_cap
xc1[31] top n7 unit_cap
xc1[30] top n7 unit_cap
xc1[29] top n7 unit_cap
xc1[28] top n7 unit_cap
xc1[27] top n7 unit_cap
xc1[26] top n7 unit_cap
xc1[25] top n7 unit_cap
xc1[24] top n7 unit_cap
xc1[23] top n7 unit_cap
xc1[22] top n7 unit_cap
xc1[21] top n7 unit_cap
xc1[20] top n7 unit_cap
xc1[19] top n7 unit_cap
xc1[18] top n7 unit_cap
xc1[17] top n7 unit_cap
xc1[16] top n7 unit_cap
xc1[15] top n7 unit_cap
xc1[14] top n7 unit_cap
xc1[13] top n7 unit_cap
xc1[12] top n7 unit_cap
xc1[11] top n7 unit_cap
xc1[10] top n7 unit_cap
xc1[9] top n7 unit_cap
xc1[8] top n7 unit_cap
xc1[7] top n7 unit_cap
xc1[6] top n7 unit_cap
xc1[5] top n7 unit_cap
xc1[4] top n7 unit_cap
xc1[3] top n7 unit_cap
xc1[2] top n7 unit_cap
xc1[1] top n7 unit_cap
xc1[0] top n7 unit_cap
**.ends

* expanding   symbol:  adc/unit_cap.sym # of pins=2
** sym_path: xschem/adc/unit_cap.sym
** sch_path: xschem/adc/unit_cap.sch
.subckt unit_cap cp cn
*.iopin cp
*.iopin cn
C1 cp cn 2.6f m=1
.ends

.end
